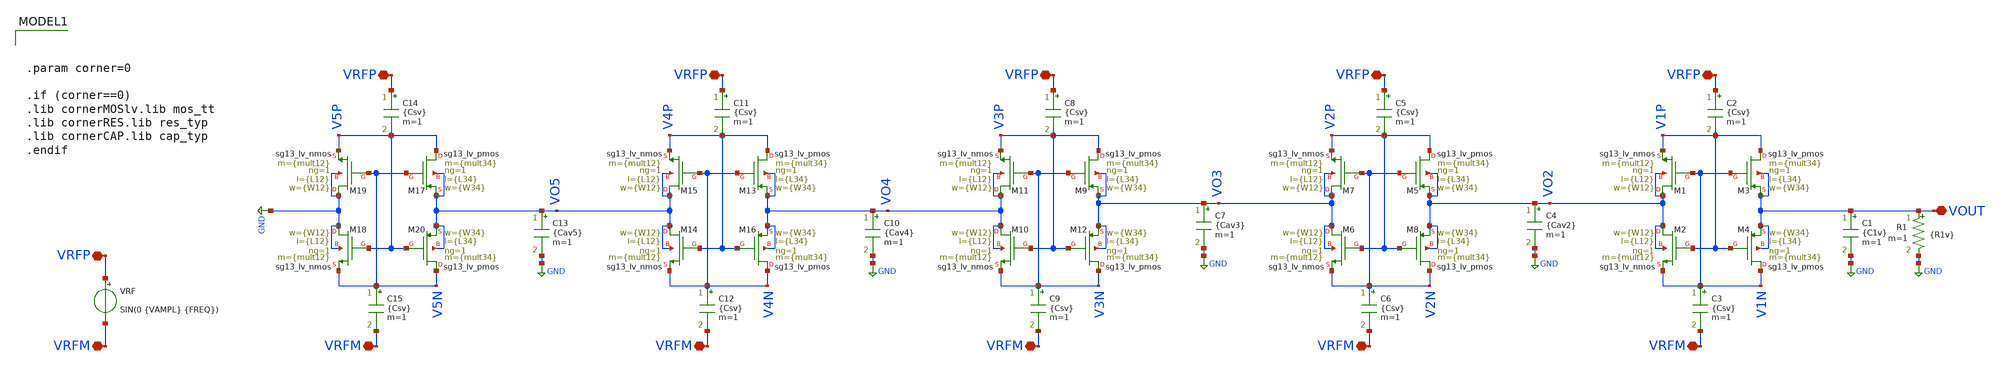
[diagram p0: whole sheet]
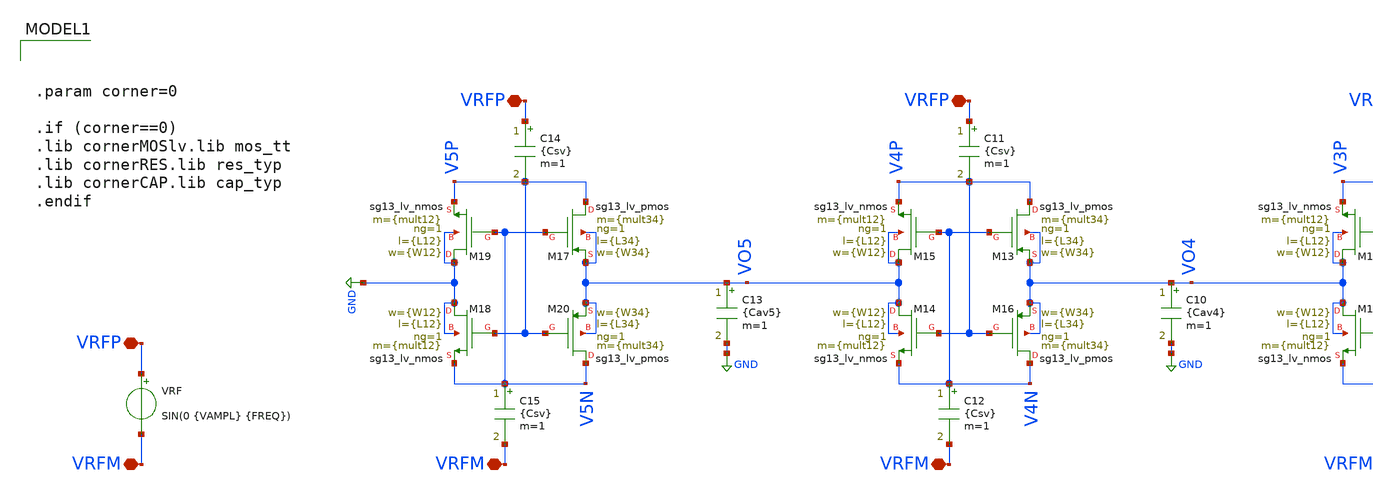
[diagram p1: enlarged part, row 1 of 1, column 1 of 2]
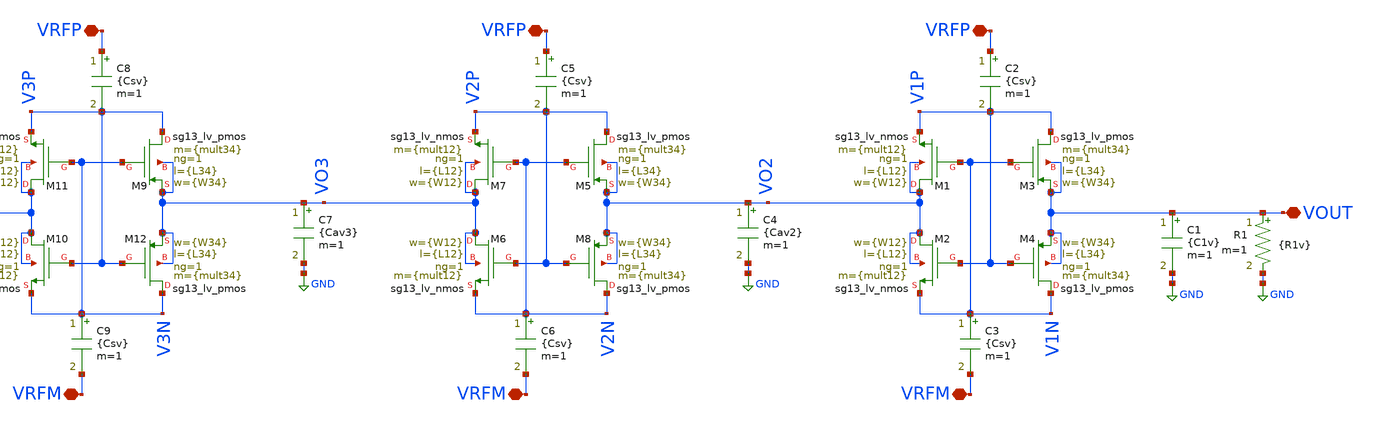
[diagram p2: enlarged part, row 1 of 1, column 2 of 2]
** sch_path: Esquematicos_Xschem/Memoria_CCDD_TRAN_MULT5.sch
**.subckt Memoria_CCDD_TRAN_MULT5 VRFP VRFM VOUT VRFP VRFM VRFP VRFM VRFP VRFM VRFP VRFM VRFP VRFM
*.iopin VRFP
*.iopin VRFM
*.iopin VOUT
*.iopin VRFP
*.iopin VRFM
*.iopin VRFP
*.iopin VRFM
*.iopin VRFP
*.iopin VRFM
*.iopin VRFP
*.iopin VRFM
*.iopin VRFP
*.iopin VRFM
XM3 V1P V1N VOUT VOUT sg13_lv_pmos w={W34} l={L34} ng=1 m={mult34} mm_ok=1
XM2 VO2 V1P V1N VO2 sg13_lv_nmos w={W12} l={L12} ng=1 m={mult12} mm_ok=1
XM1 VO2 V1N V1P VO2 sg13_lv_nmos w={W12} l={L12} ng=1 m={mult12} mm_ok=1
XM4 V1N V1P VOUT VOUT sg13_lv_pmos w={W34} l={L34} ng=1 m={mult34} mm_ok=1
R1 VOUT GND {R1v} m=1
C1 VOUT GND {C1v} m=1
VRF VRFP VRFM SIN(0 {VAMPL} {FREQ})
.save i(vrf)
C2 VRFP V1P {Csv} m=1
C3 V1N VRFM {Csv} m=1
XM5 V2P V2N VO2 VO2 sg13_lv_pmos w={W34} l={L34} ng=1 m={mult34} mm_ok=1
XM6 VO3 V2P V2N VO3 sg13_lv_nmos w={W12} l={L12} ng=1 m={mult12} mm_ok=1
XM7 VO3 V2N V2P VO3 sg13_lv_nmos w={W12} l={L12} ng=1 m={mult12} mm_ok=1
XM8 V2N V2P VO2 VO2 sg13_lv_pmos w={W34} l={L34} ng=1 m={mult34} mm_ok=1
C4 VO2 GND {Cav2} m=1
C5 VRFP V2P {Csv} m=1
C6 V2N VRFM {Csv} m=1
XM9 V3P V3N VO3 VO3 sg13_lv_pmos w={W34} l={L34} ng=1 m={mult34} mm_ok=1
XM10 VO4 V3P V3N VO4 sg13_lv_nmos w={W12} l={L12} ng=1 m={mult12} mm_ok=1
XM11 VO4 V3N V3P VO4 sg13_lv_nmos w={W12} l={L12} ng=1 m={mult12} mm_ok=1
XM12 V3N V3P VO3 VO3 sg13_lv_pmos w={W34} l={L34} ng=1 m={mult34} mm_ok=1
C7 VO3 GND {Cav3} m=1
C8 VRFP V3P {Csv} m=1
C9 V3N VRFM {Csv} m=1
XM13 V4P V4N VO4 VO4 sg13_lv_pmos w={W34} l={L34} ng=1 m={mult34} mm_ok=1
XM14 VO5 V4P V4N VO5 sg13_lv_nmos w={W12} l={L12} ng=1 m={mult12} mm_ok=1
XM15 VO5 V4N V4P VO5 sg13_lv_nmos w={W12} l={L12} ng=1 m={mult12} mm_ok=1
XM16 V4N V4P VO4 VO4 sg13_lv_pmos w={W34} l={L34} ng=1 m={mult34} mm_ok=1
C10 VO4 GND {Cav4} m=1
C11 VRFP V4P {Csv} m=1
C12 V4N VRFM {Csv} m=1
XM17 V5P V5N VO5 VO5 sg13_lv_pmos w={W34} l={L34} ng=1 m={mult34} mm_ok=1
XM18 GND V5P V5N GND sg13_lv_nmos w={W12} l={L12} ng=1 m={mult12} mm_ok=1
XM19 GND V5N V5P GND sg13_lv_nmos w={W12} l={L12} ng=1 m={mult12} mm_ok=1
XM20 V5N V5P VO5 VO5 sg13_lv_pmos w={W34} l={L34} ng=1 m={mult34} mm_ok=1
C13 VO5 GND {Cav5} m=1
C14 VRFP V5P {Csv} m=1
C15 V5N VRFM {Csv} m=1
**** begin user architecture code



.option wnflag=1
.savecurrents

* =============================
* PARAMETROS DE SIMULACION
* =============================

**** Parametros PMOS M3 y M4
.param L34 = 0.2u
.param W34 = 1.78u
.param mult34 = 20

**** Parametros NMOS M1 y M2
.param L12 = 0.2u
.param W12 = 0.6u
.param mult12 = 20

* Parametros PMOS M1
*.param Lval1 = 0.13u
*.param Wval1 = 0.15u
*.param mult1 = 5

* Parametros NMOS M2
*.param Lval2 = 1u
*.param Wval2 = 0.15u
*.param mult2 = 1

* Parametros NMOS M3
*.param Lval3 = 1u
*.param Wval3 = 0.15u
*.param mult3 = 1

* Parametros PMOS M4
*.param Lval4 = 1u
*.param Wval4 = 0.15u
*.param mult4 = 1

**** Parametros de Carga
.param C1v = 1p
.ic V(VOUT) = 0
.param R1v = 100k

**** Parametros de Acople
.param Csv = 1p
.param Cav2 = 2*1p
.param Cav3 = 3*1p
.param Cav4 = 4*1p
.param Cav5 = 5*1p

**** Parametros Fuente Sinusoidal
.param VAMPL = 0.1      ; Amplitud (V)
.param VOFFS = 0         ; Valor medio (V)
.param FREQ  = 900MEG        ; Frecuencia (Hz)
.param PHASE = 0         ; Fase1 (grados)








.option wnflag=1
.savecurrents

* ==============================================
* BLOQUE DE CONTROL NGSPICE
* ==============================================
.control

**** Compatibilidad y Color
  set filetype = ascii
  set color0 = white

**** Inicializacion de Parametro While
  let k = 0
  let start_VRF = 0.3
  let stop_VRF = 1.2
  let delta_VRF = 0.1
  let VRF_act = start_VRF

**** Inicializacion Constantes para Calculos
  let i = 0
  let IDmax = 0
  let IGmax = 0
  let VDSmax = 0
  let VGSmax = 0

**** Variables Exteriores


* ==============================================
* Inicio del While
* ==============================================
  while VRF_act le stop_VRF + 2*delta_VRF
    if k = 1
      tran 20p 500n UIC
    end
    alterparam VAMPL = $&VRF_act
    reset

* -----------------------------
* Almacenamiento de Variables
* -----------------------------
    save all

    **** M2
    save @n.xm2.nsg13_lv_nmos[ids]
    save @n.xm2.nsg13_lv_nmos[igs]
    save @n.xm2.nsg13_lv_nmos[gm]
    save @n.xm2.nsg13_lv_nmos[gds]
    save @n.xm2.nsg13_lv_nmos[vth]

    **** M6
    save @n.xm6.nsg13_lv_nmos[ids]
    save @n.xm6.nsg13_lv_nmos[igs]
    save @n.xm6.nsg13_lv_nmos[gm]
    save @n.xm6.nsg13_lv_nmos[gds]
    save @n.xm6.nsg13_lv_nmos[vth]

    **** M10
    save @n.xm10.nsg13_lv_nmos[ids]
    save @n.xm10.nsg13_lv_nmos[igs]
    save @n.xm10.nsg13_lv_nmos[gm]
    save @n.xm10.nsg13_lv_nmos[gds]
    save @n.xm10.nsg13_lv_nmos[vth]

    **** M14
    save @n.xm14.nsg13_lv_nmos[ids]
    save @n.xm14.nsg13_lv_nmos[igs]
    save @n.xm14.nsg13_lv_nmos[gm]
    save @n.xm14.nsg13_lv_nmos[gds]
    save @n.xm14.nsg13_lv_nmos[vth]

    **** M18
    save @n.xm18.nsg13_lv_nmos[ids]
    save @n.xm18.nsg13_lv_nmos[igs]
    save @n.xm18.nsg13_lv_nmos[gm]
    save @n.xm18.nsg13_lv_nmos[gds]
    save @n.xm18.nsg13_lv_nmos[vth]

    **** Fuente de Voltaje
    save @VRF[i]
    save @VRF[p]

    **** Carga
    save R1[i]
    save C1[i]

* ----------------------------------------------
* Definicion de Varriables Internas
* ----------------------------------------------
    if k = 1

      **** M2
      let ids2 = @n.xm2.nsg13_lv_nmos[ids]
      let igs2 = @n.xm2.nsg13_lv_nmos[igs]
      let gm2 = @n.xm2.nsg13_lv_nmos[gm]
      let gds2 =  @n.xm2.nsg13_lv_nmos[gds]
      let vth2 = @n.xm2.nsg13_lv_nmos[vth]
      let VDS2 = V1N - VO2
      let VGS2 = V1P - VO2

      **** M6
      let ids6 = @n.xm6.nsg13_lv_nmos[ids]
      let igs6 = @n.xm6.nsg13_lv_nmos[igs]
      let gm6 = @n.xm6.nsg13_lv_nmos[gm]
      let gds6 =  @n.xm6.nsg13_lv_nmos[gds]
      let vth6 = @n.xm6.nsg13_lv_nmos[vth]
      let VDS6 = V2N - VO3
      let VGS6 = V2P - VO3

      **** M10
      let ids10 = @n.xm10.nsg13_lv_nmos[ids]
      let igs10 = @n.xm10.nsg13_lv_nmos[igs]
      let gm10 = @n.xm10.nsg13_lv_nmos[gm]
      let gds10 =  @n.xm10.nsg13_lv_nmos[gds]
      let vth10 = @n.xm10.nsg13_lv_nmos[vth]
      let VDS10 = V3N - VO4
      let VGS10 = V3P - VO4

      **** M14
      let ids14 = @n.xm14.nsg13_lv_nmos[ids]
      let igs14 = @n.xm14.nsg13_lv_nmos[igs]
      let gm14 = @n.xm14.nsg13_lv_nmos[gm]
      let gds14 =  @n.xm14.nsg13_lv_nmos[gds]
      let vth14 = @n.xm14.nsg13_lv_nmos[vth]
      let VDS14 = V4N - VO5
      let VGS14 = V4P - VO5

      **** M18
      let ids18 = @n.xm18.nsg13_lv_nmos[ids]
      let igs18 = @n.xm18.nsg13_lv_nmos[igs]
      let gm18 = @n.xm18.nsg13_lv_nmos[gm]
      let gds18 =  @n.xm18.nsg13_lv_nmos[gds]
      let vth18 = @n.xm18.nsg13_lv_nmos[vth]
      let VDS18 = V5N - 0
      let VGS18 = V5P - 0

      **** Fuente de Voltaje
      let IRF = @VRF[i]
      let PRF = @VRF[p]
      let VRF = VRFP - VRFM

      **** Carga
      let IC = @C1[i]
      let IR = @R1[i]
      let IRC = IC + IR
      let PR = IR * VOUT
    end


* ==============================================
* RESULTADOS
* ==============================================

* -----------------------------
* Graficas de la Simulacion
* -----------------------------
    if k = 1
    **** Fuente
    *plot VRF vs time
    *plot IRF vs time

    **** Carga
    plot VOUT VRF vs time
    *plot IRC vs time
    *plot avg(PR/PRF)
    end

* -----------------------------
* Registro de Datos
* -----------------------------
    remzerovec
    write Memoria_CCDD2_TRAN_MULT5_L00-20_W00-60_R100k_M20_C01-00.csv time VRF IRF VOUT VO2 VO3 VO4
+ VO5 IC IR VDS2 VDS6 VDS10 VDS14 VDS18 VGS2 VGS6 VGS10 VGS14 VGS18 ids2 ids6 ids10 ids14 ids18 igs2 igs6
+ igs10 igs14 igs18


* ==============================================
* CIERRE DE WHILE
* ==============================================
    **** Definicion de proximo valor (while)
    let VRF_act = VRF_act + delta_VRF
    let k = 1
    set appendwrite

  end

.endc




.param corner=0

.if (corner==0)
.lib cornerMOSlv.lib mos_tt
.lib cornerRES.lib res_typ
.lib cornerCAP.lib cap_typ
.endif

**** end user architecture code
**.ends
.GLOBAL GND
.end
